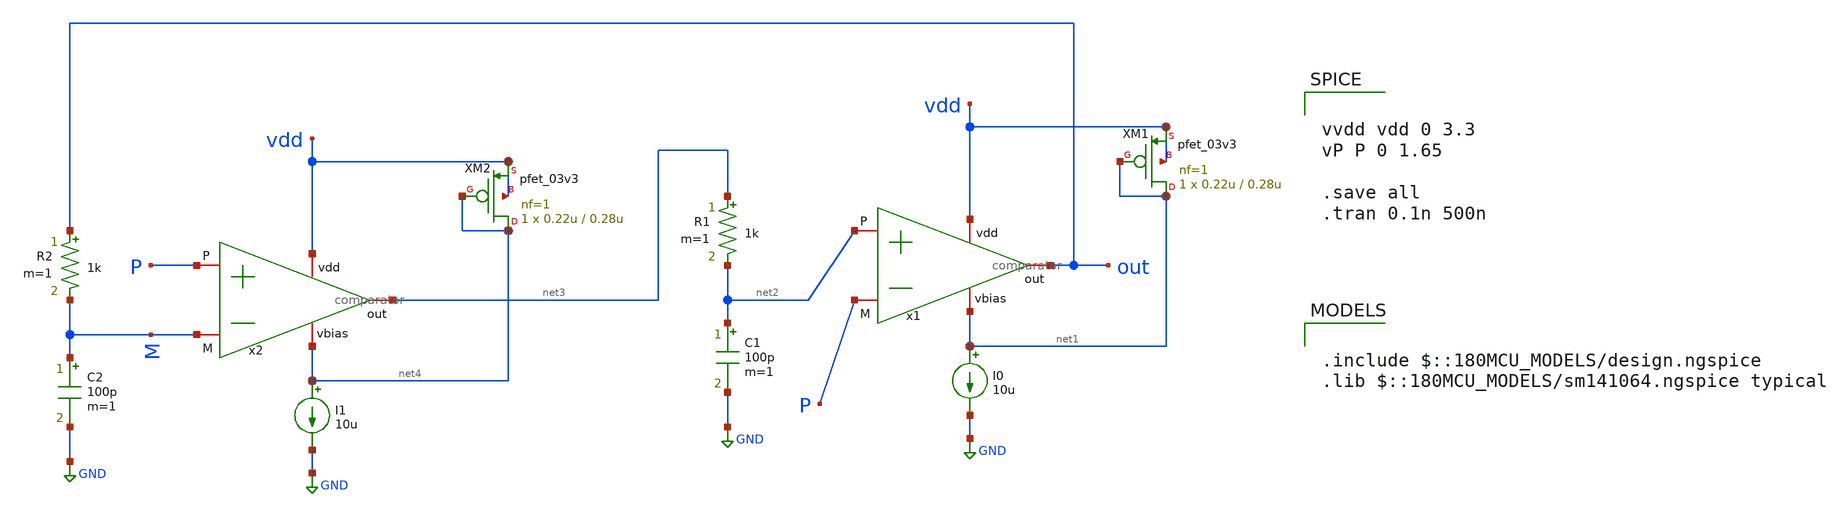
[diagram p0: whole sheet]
** sch_path: Clock_Reference/symbols_clock/untitled-1.sch
**.subckt untitled-1
x1 vdd net1 net2 P out comparator
XM1 net1 net1 vdd vdd pfet_03v3 L=0.28u W=0.22u nf=1 ad='int((nf+1)/2) * W/nf * 0.18u' as='int((nf+2)/2) * W/nf * 0.18u'
+ pd='2*int((nf+1)/2) * (W/nf + 0.18u)' ps='2*int((nf+2)/2) * (W/nf + 0.18u)' nrd='0.18u / W' nrs='0.18u / W'
+ sa=0 sb=0 sd=0 m=1
I0 net1 GND 10u
R1 net3 net2 1k m=1
C1 net2 GND 100p m=1
x2 vdd net4 P M net3 comparator
XM2 net4 net4 vdd vdd pfet_03v3 L=0.28u W=0.22u nf=1 ad='int((nf+1)/2) * W/nf * 0.18u' as='int((nf+2)/2) * W/nf * 0.18u'
+ pd='2*int((nf+1)/2) * (W/nf + 0.18u)' ps='2*int((nf+2)/2) * (W/nf + 0.18u)' nrd='0.18u / W' nrs='0.18u / W'
+ sa=0 sb=0 sd=0 m=1
I1 net4 GND 10u
R2 out M 1k m=1
C2 M GND 100p m=1
**** begin user architecture code

.include $::180MCU_MODELS/design.ngspice
.lib $::180MCU_MODELS/sm141064.ngspice typical



vvdd vdd 0 3.3
vP P 0 1.65

.save all
.tran 0.1n 500n


**** end user architecture code
**.ends
.GLOBAL GND
.end
